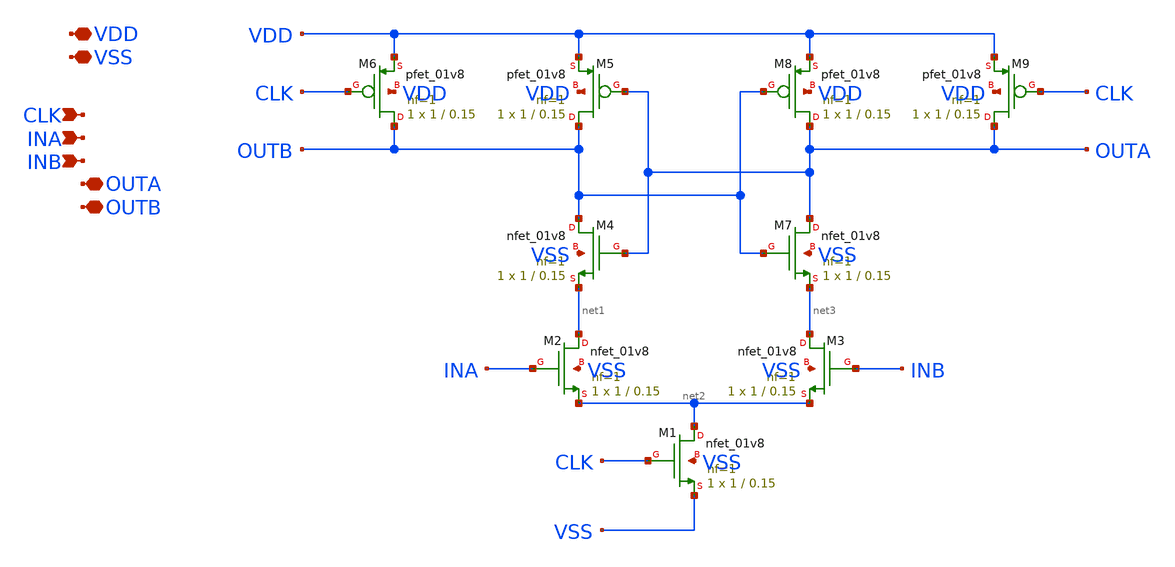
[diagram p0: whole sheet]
** sch_path: comp1.sch
**.subckt comp1 VSS VDD OUTB OUTA INB INA CLK
*.iopin VSS
*.iopin VDD
*.iopin OUTB
*.iopin OUTA
*.ipin INB
*.ipin INA
*.ipin CLK
XM1 net2 CLK VSS VSS sky130_fd_pr__nfet_01v8 L=0.15 W=1 nf=1 ad='int((nf+1)/2) * W/nf * 0.29' as='int((nf+2)/2) * W/nf * 0.29'
+ pd='2*int((nf+1)/2) * (W/nf + 0.29)' ps='2*int((nf+2)/2) * (W/nf + 0.29)' nrd='0.29 / W' nrs='0.29 / W'
+ sa=0 sb=0 sd=0 mult=1 m=1
XM2 net1 INA net2 VSS sky130_fd_pr__nfet_01v8 L=0.15 W=1 nf=1 ad='int((nf+1)/2) * W/nf * 0.29' as='int((nf+2)/2) * W/nf * 0.29'
+ pd='2*int((nf+1)/2) * (W/nf + 0.29)' ps='2*int((nf+2)/2) * (W/nf + 0.29)' nrd='0.29 / W' nrs='0.29 / W'
+ sa=0 sb=0 sd=0 mult=1 m=1
XM4 OUTB OUTA net1 VSS sky130_fd_pr__nfet_01v8 L=0.15 W=1 nf=1 ad='int((nf+1)/2) * W/nf * 0.29' as='int((nf+2)/2) * W/nf * 0.29'
+ pd='2*int((nf+1)/2) * (W/nf + 0.29)' ps='2*int((nf+2)/2) * (W/nf + 0.29)' nrd='0.29 / W' nrs='0.29 / W'
+ sa=0 sb=0 sd=0 mult=1 m=1
XM5 OUTB OUTA VDD VDD sky130_fd_pr__pfet_01v8 L=0.15 W=1 nf=1 ad='int((nf+1)/2) * W/nf * 0.29' as='int((nf+2)/2) * W/nf * 0.29'
+ pd='2*int((nf+1)/2) * (W/nf + 0.29)' ps='2*int((nf+2)/2) * (W/nf + 0.29)' nrd='0.29 / W' nrs='0.29 / W'
+ sa=0 sb=0 sd=0 mult=1 m=1
XM6 OUTB CLK VDD VDD sky130_fd_pr__pfet_01v8 L=0.15 W=1 nf=1 ad='int((nf+1)/2) * W/nf * 0.29' as='int((nf+2)/2) * W/nf * 0.29'
+ pd='2*int((nf+1)/2) * (W/nf + 0.29)' ps='2*int((nf+2)/2) * (W/nf + 0.29)' nrd='0.29 / W' nrs='0.29 / W'
+ sa=0 sb=0 sd=0 mult=1 m=1
XM3 net3 INB net2 VSS sky130_fd_pr__nfet_01v8 L=0.15 W=1 nf=1 ad='int((nf+1)/2) * W/nf * 0.29' as='int((nf+2)/2) * W/nf * 0.29'
+ pd='2*int((nf+1)/2) * (W/nf + 0.29)' ps='2*int((nf+2)/2) * (W/nf + 0.29)' nrd='0.29 / W' nrs='0.29 / W'
+ sa=0 sb=0 sd=0 mult=1 m=1
XM7 OUTA OUTB net3 VSS sky130_fd_pr__nfet_01v8 L=0.15 W=1 nf=1 ad='int((nf+1)/2) * W/nf * 0.29' as='int((nf+2)/2) * W/nf * 0.29'
+ pd='2*int((nf+1)/2) * (W/nf + 0.29)' ps='2*int((nf+2)/2) * (W/nf + 0.29)' nrd='0.29 / W' nrs='0.29 / W'
+ sa=0 sb=0 sd=0 mult=1 m=1
XM8 OUTA OUTB VDD VDD sky130_fd_pr__pfet_01v8 L=0.15 W=1 nf=1 ad='int((nf+1)/2) * W/nf * 0.29' as='int((nf+2)/2) * W/nf * 0.29'
+ pd='2*int((nf+1)/2) * (W/nf + 0.29)' ps='2*int((nf+2)/2) * (W/nf + 0.29)' nrd='0.29 / W' nrs='0.29 / W'
+ sa=0 sb=0 sd=0 mult=1 m=1
XM9 OUTA CLK VDD VDD sky130_fd_pr__pfet_01v8 L=0.15 W=1 nf=1 ad='int((nf+1)/2) * W/nf * 0.29' as='int((nf+2)/2) * W/nf * 0.29'
+ pd='2*int((nf+1)/2) * (W/nf + 0.29)' ps='2*int((nf+2)/2) * (W/nf + 0.29)' nrd='0.29 / W' nrs='0.29 / W'
+ sa=0 sb=0 sd=0 mult=1 m=1
**.ends
.end
